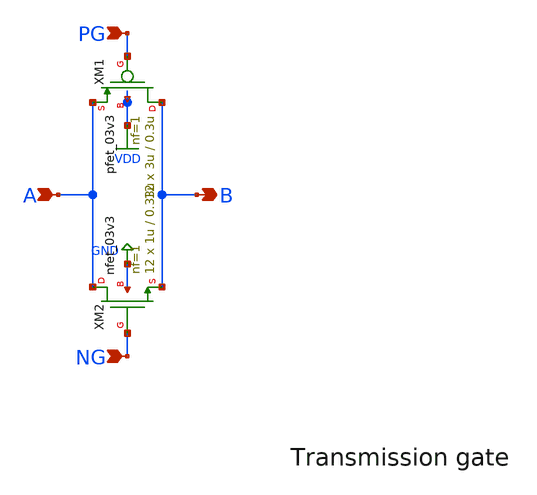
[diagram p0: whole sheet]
** sch_path: schematic/tmg.sch
**.subckt tmg B A PG NG
*.opin B
*.ipin A
*.ipin PG
*.ipin NG
XM1 B PG A VDD pfet_03v3 L=0.3u W=3u nf=1 ad='int((nf+1)/2) * W/nf * 0.18u' as='int((nf+2)/2) * W/nf * 0.18u'
+ pd='2*int((nf+1)/2) * (W/nf + 0.18u)' ps='2*int((nf+2)/2) * (W/nf + 0.18u)' nrd='0.18u / W' nrs='0.18u / W'
+ sa=0 sb=0 sd=0 m=12
XM2 A NG B GND nfet_03v3 L=0.33u W=1u nf=1 ad='int((nf+1)/2) * W/nf * 0.18u' as='int((nf+2)/2) * W/nf * 0.18u'
+ pd='2*int((nf+1)/2) * (W/nf + 0.18u)' ps='2*int((nf+2)/2) * (W/nf + 0.18u)' nrd='0.18u / W' nrs='0.18u / W'
+ sa=0 sb=0 sd=0 m=12
**.ends
.GLOBAL GND
.GLOBAL VDD
.end
